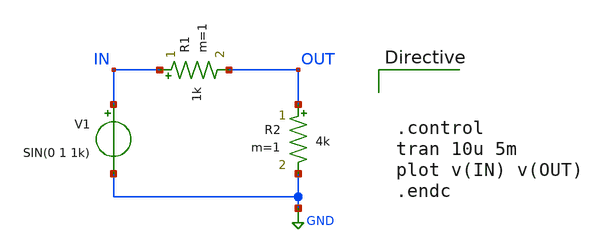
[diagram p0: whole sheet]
** sch_path: designs/sophiazhu/session_0/res_div.sch
**.subckt res_div
R1 IN OUT 1k m=1
R2 OUT GND 4k m=1
V1 IN GND SIN(0 1 1k)
**** begin user architecture code



.control
tran 10u 5m
plot v(IN) v(OUT)
.endc



**** end user architecture code
**.ends
.GLOBAL GND
.end
